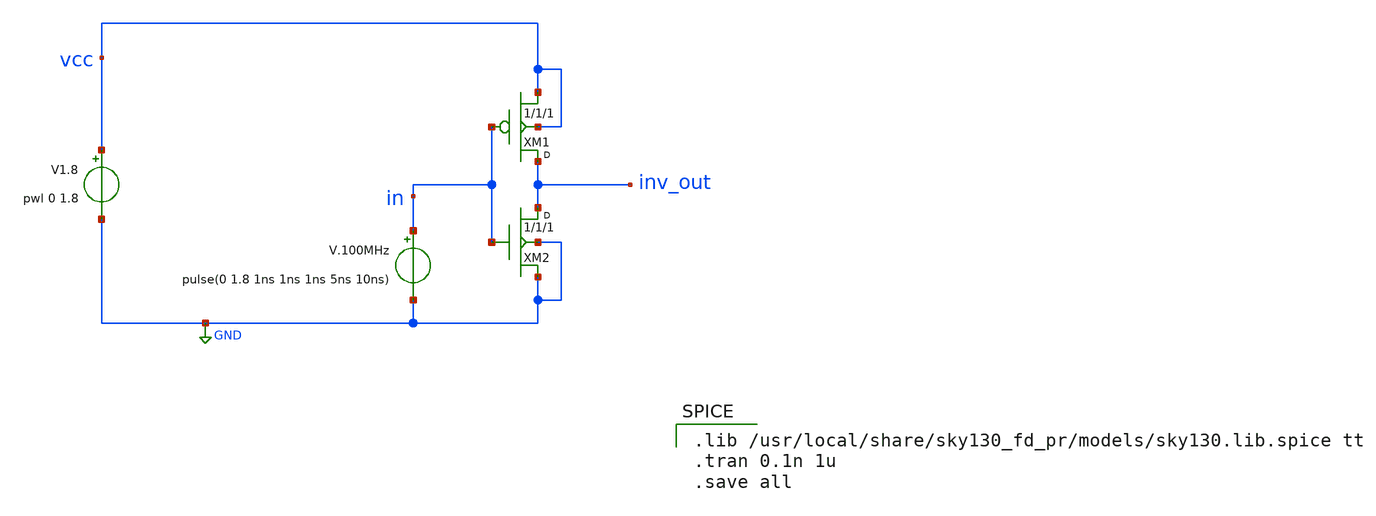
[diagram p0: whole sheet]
** sch_path: schematic/xschem/basic-inverter.sch
**.subckt basic-inverter
V.100MHz in GND pulse(0 1.8 1ns 1ns 1ns 5ns 10ns)
XM1 inv_out in vcc vcc sky130_fd_pr__pfet_01v8 w=1 l=1 m=1
XM2 inv_out in GND GND sky130_fd_pr__nfet_01v8 w=1 l=1 m=1
V1.8 vcc GND pwl 0 1.8
**** begin user architecture code

.lib /usr/local/share/sky130_fd_pr/models/sky130.lib.spice tt
.tran 0.1n 1u
.save all

**** end user architecture code
**.ends
.GLOBAL GND
.end
